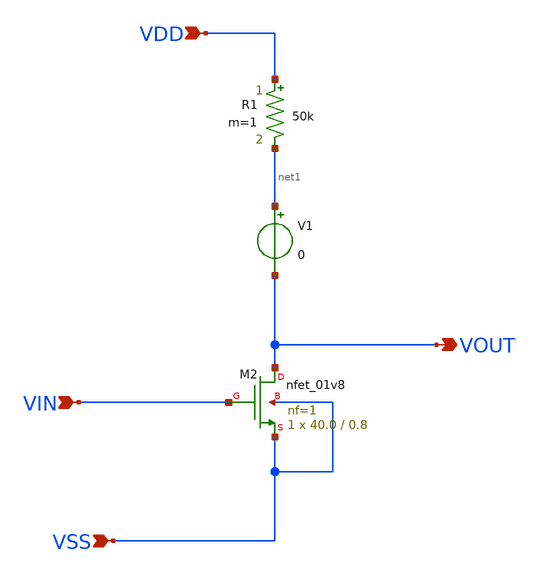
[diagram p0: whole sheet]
** sch_path: lelo_ex1_sky130a/design/LELO_EX1_SKY130A/LELO_EX1.sch
**.subckt LELO_EX1 VOUT VSS VDD VIN
*.opin VOUT
*.ipin VSS
*.ipin VDD
*.ipin VIN
XM2 VOUT VIN VSS VSS sky130_fd_pr__nfet_01v8 L=0.8 W=40.0 nf=1 ad='int((1 + 1)/2) * 40.0 / 1 * 0.29'
+ as='int((1 + 2)/2) * 40.0 / 1 * 0.29' pd='2*int((1 + 1)/2) * (40.0 / 1 + 0.29)' ps='2*int((1 + 2)/2) * (40.0 / 1 + 0.29)'
+ nrd='0.29 / 40.0 ' nrs='0.29 / 40.0 ' sa=0 sb=0 sd=0 mult=1 m=1
V1 net1 VOUT 0
.save i(v1)
R1 VDD net1 50k m=1
**.ends
.end
